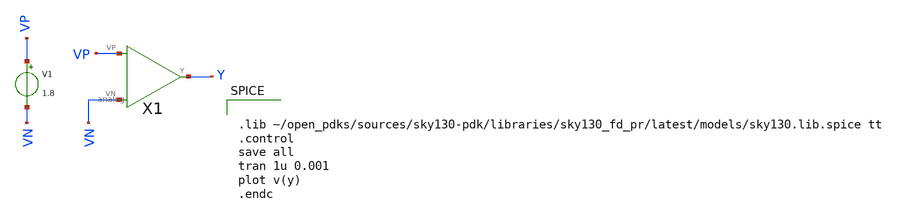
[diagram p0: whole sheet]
** sch_path: Week 3/Week 3/xschem 2/analog_tb.sch
**.subckt analog_tb
X1 VN VP Y analog
V1 VP VN 1.8
**** begin user architecture code


.lib ~/open_pdks/sources/sky130-pdk/libraries/sky130_fd_pr/latest/models/sky130.lib.spice tt
.control
save all
tran 1u 0.001
plot v(y)
.endc

**** end user architecture code
**.ends
.end
